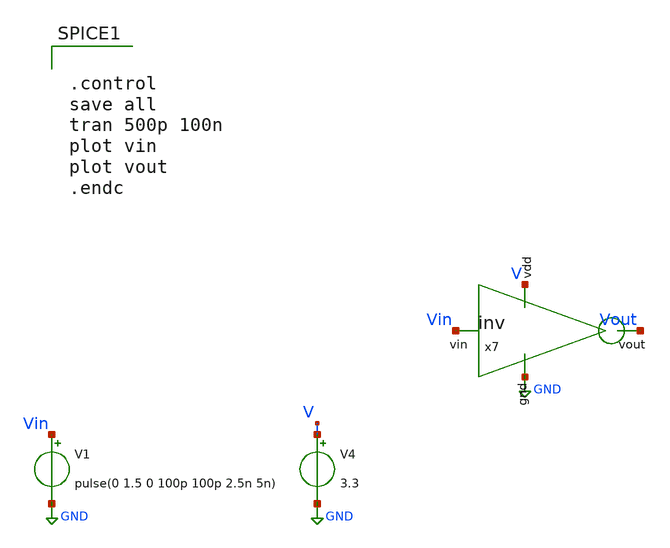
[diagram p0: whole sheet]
** sch_path: testbench/inverter__tb.sch
**.subckt inverter__tb
V1 Vin GND pulse(0 1.5 0 100p 100p 2.5n 5n)
V4 V GND 3.3
x7 V GND Vout Vin inv cl=0.28u wp=0.44u wn=0.22u
**** begin user architecture code


.control
save all
tran 500p 100n
plot vin
plot vout
.endc


.include /foss/pdks/gf180mcuC/libs.tech/ngspice/design.ngspice
.lib /foss/pdks/gf180mcuC/libs.tech/ngspice/sm141064.ngspice typical

**** end user architecture code
**.ends

* expanding   symbol:  SAR_ADC/SAR_ADC_gf180/xschem/spice/inv.sym # of pins=4
** sym_path: SAR_ADC/SAR_ADC_gf180/xschem/spice/inv.sym
** sch_path: SAR_ADC/SAR_ADC_gf180/xschem/spice/inv.sch
.subckt inv vdd gnd vout vin  cl=0.28u wp=0.44u wn=0.22u
*.ipin gnd
*.ipin vdd
*.ipin vin
*.opin vout
XM1 gnd vin vout gnd nfet_03v3 L=0.28u W=4u nf=1 ad='int((nf+1)/2) * W/nf * 0.18u' as='int((nf+2)/2) * W/nf * 0.18u'
+ pd='2*int((nf+1)/2) * (W/nf + 0.18u)' ps='2*int((nf+2)/2) * (W/nf + 0.18u)' nrd='0.18u / W' nrs='0.18u / W'
+ sa=0 sb=0 sd=0 m=1
XM2 vdd vin vout vdd pfet_03v3 L=0.28u W=4u nf=1 ad='int((nf+1)/2) * W/nf * 0.18u' as='int((nf+2)/2) * W/nf * 0.18u'
+ pd='2*int((nf+1)/2) * (W/nf + 0.18u)' ps='2*int((nf+2)/2) * (W/nf + 0.18u)' nrd='0.18u / W' nrs='0.18u / W'
+ sa=0 sb=0 sd=0 m=1
.ends

.GLOBAL GND
.end
